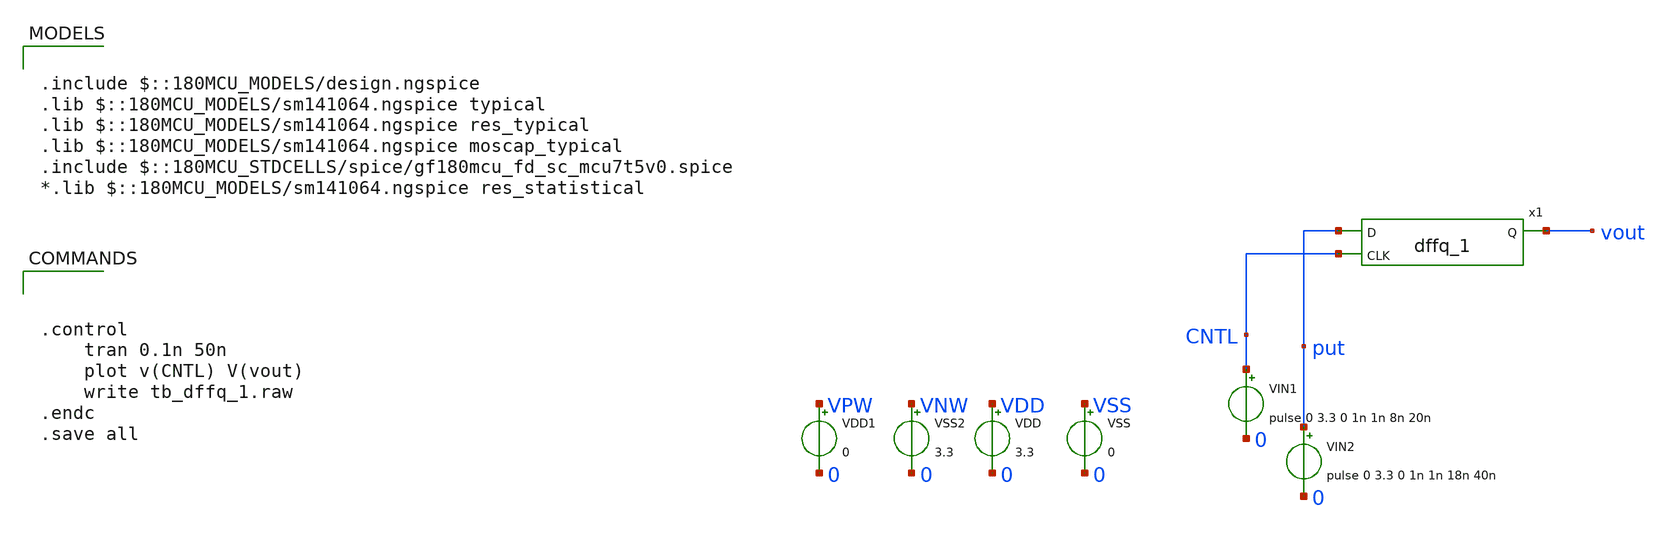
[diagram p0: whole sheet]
** sch_path: DAC/xschem/std_cell/tb/tb_dffq_1.sch
**.subckt tb_dffq_1
VIN1 CNTL 0 pulse 0 3.3 0 1n 1n 8n 20n
VIN2 put 0 pulse 0 3.3 0 1n 1n 18n 40n
VDD VDD 0 3.3
VSS VSS 0 0
VDD1 VPW 0 0
VSS2 VNW 0 3.3
x1 put CNTL vout VDD VNW VPW VSS gf180mcu_fd_sc_mcu7t5v0__dffq_1
**** begin user architecture code



.control
    tran 0.1n 50n
    plot v(CNTL) V(vout)
    write tb_dffq_1.raw
.endc
.save all




.include $::180MCU_MODELS/design.ngspice
.lib $::180MCU_MODELS/sm141064.ngspice typical
.lib $::180MCU_MODELS/sm141064.ngspice res_typical
.lib $::180MCU_MODELS/sm141064.ngspice moscap_typical
.include $::180MCU_STDCELLS/spice/gf180mcu_fd_sc_mcu7t5v0.spice
*.lib $::180MCU_MODELS/sm141064.ngspice res_statistical

**** end user architecture code
**.ends
.end
